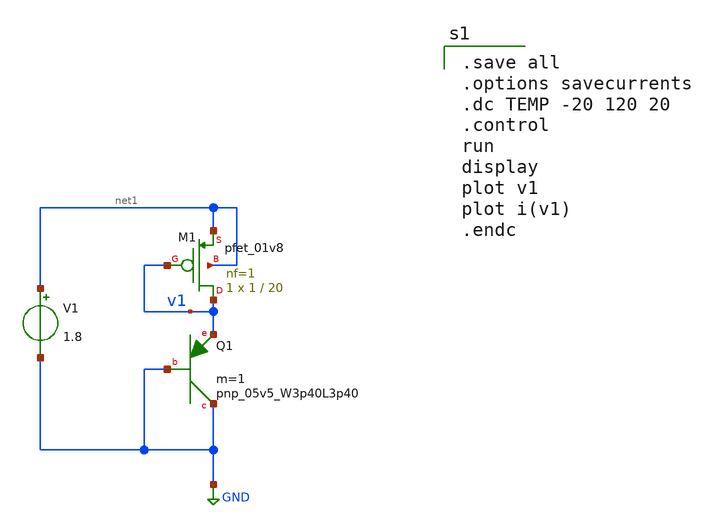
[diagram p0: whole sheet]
** sch_path: SKY130/xschem/cmos_vref/Y.Ji_JSSC2019/s1_ctat.sch
**.subckt s1_ctat
XQ1 GND GND v1 sky130_fd_pr__pnp_05v5_W3p40L3p40 m=1
V1 net1 GND 1.8
XM1 v1 v1 net1 net1 sky130_fd_pr__pfet_01v8 L=20 W=1 nf=1 ad='int((nf+1)/2) * W/nf * 0.29' as='int((nf+2)/2) * W/nf * 0.29'
+ pd='2*int((nf+1)/2) * (W/nf + 0.29)' ps='2*int((nf+2)/2) * (W/nf + 0.29)' nrd='0.29 / W' nrs='0.29 / W'
+ sa=0 sb=0 sd=0 mult=1 m=1
**** begin user architecture code
.lib $::SKYWATER_MODELS/sky130.lib.spice tt
.include $::PDKPATH/libs.ref/sky130_fd_sc_hvl/spice/sky130_fd_sc_hvl.spice

.save all
.options savecurrents
.dc TEMP -20 120 20
.control
run
display
plot v1
plot i(v1)
.endc


**** end user architecture code
**.ends
.GLOBAL GND
.end
